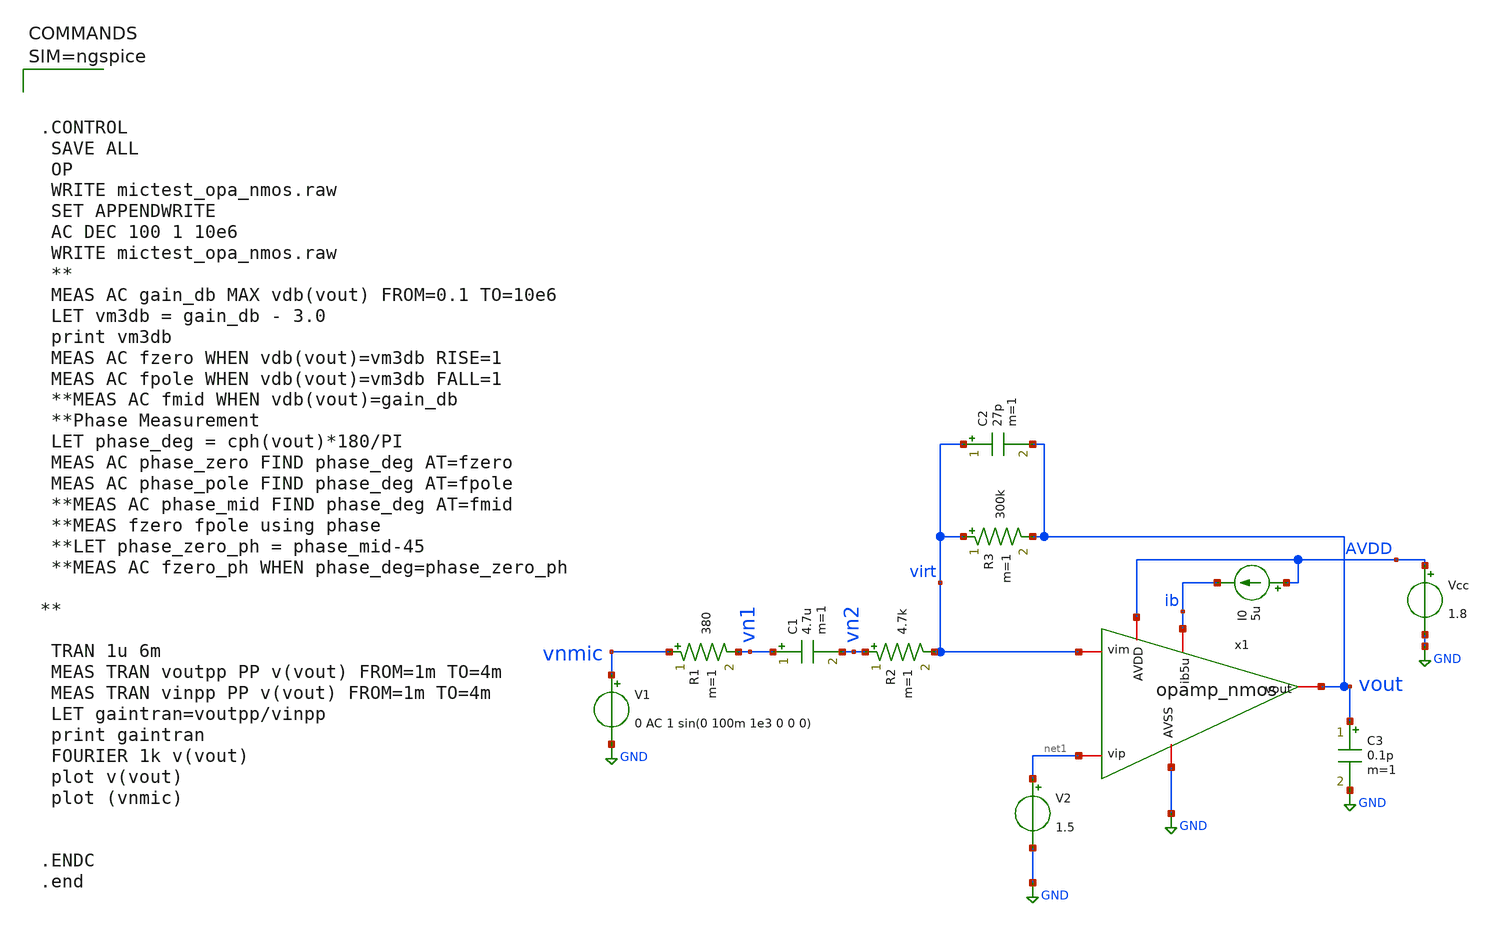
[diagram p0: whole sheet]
** sch_path: xschem/mictest_opa_nmos.sch
**.subckt mictest_opa_nmos
V1 vnmic GND 0 AC 1 sin(0 100m 1e3 0 0 0)
C1 vn1 vn2 4.7u m=1
R1 vnmic vn1 380 m=1
R2 vn2 virt 4.7k m=1
R3 virt vout 300k m=1
C2 virt vout 27p m=1
C3 vout GND 0.1p m=1
V2 net1 GND 1.5
x1 net1 GND AVDD virt ib vout opamp_nmos
Vcc AVDD GND 1.8
I0 AVDD ib 5u
**** begin user architecture code




.CONTROL
 SAVE ALL
 OP
 WRITE mictest_opa_nmos.raw
 SET APPENDWRITE
 AC DEC 100 1 10e6
 WRITE mictest_opa_nmos.raw
 **
 MEAS AC gain_db MAX vdb(vout) FROM=0.1 TO=10e6
 LET vm3db = gain_db - 3.0
 print vm3db
 MEAS AC fzero WHEN vdb(vout)=vm3db RISE=1
 MEAS AC fpole WHEN vdb(vout)=vm3db FALL=1
 **MEAS AC fmid WHEN vdb(vout)=gain_db
 **Phase Measurement
 LET phase_deg = cph(vout)*180/PI
 MEAS AC phase_zero FIND phase_deg AT=fzero
 MEAS AC phase_pole FIND phase_deg AT=fpole
 **MEAS AC phase_mid FIND phase_deg AT=fmid
 **MEAS fzero fpole using phase
 **LET phase_zero_ph = phase_mid-45
 **MEAS AC fzero_ph WHEN phase_deg=phase_zero_ph

**

 TRAN 1u 6m
 MEAS TRAN voutpp PP v(vout) FROM=1m TO=4m
 MEAS TRAN vinpp PP v(vout) FROM=1m TO=4m
 LET gaintran=voutpp/vinpp
 print gaintran
 FOURIER 1k v(vout)
 plot v(vout)
 plot (vnmic)


.ENDC
.end




** opencircuitdesign pdks install
.lib $::SKYWATER_MODELS/sky130.lib.spice tt

**** end user architecture code
**.ends

* expanding   symbol:  opamp_nmos.sym # of pins=6
** sym_path: xschem/opamp_nmos.sym
** sch_path: xschem/opamp_nmos.sch
.subckt opamp_nmos vip AVSS AVDD vim ib5u vout
*.iopin vip
*.iopin vim
*.iopin vout
*.iopin AVDD
*.iopin ib5u
*.iopin AVSS
XMip vom vip net1 net1 sky130_fd_pr__nfet_01v8_lvt L=2 W=5 nf=1 ad='int((1 + 1)/2) * 5 / 1 * 0.29' as='int((1 + 2)/2) * 5 / 1 * 0.29'
+ pd='2*int((1 + 1)/2) * (5 / 1 + 0.29)' ps='2*int((1 + 2)/2) * (5 / 1 + 0.29)' nrd='0.29 / 5 ' nrs='0.29 / 5 '
+ sa=0 sb=0 sd=0 mult=4 m=4
XMim vout vim net1 net1 sky130_fd_pr__nfet_01v8_lvt L=2 W=5 nf=1 ad='int((1 + 1)/2) * 5 / 1 * 0.29' as='int((1 + 2)/2) * 5 / 1 * 0.29'
+ pd='2*int((1 + 1)/2) * (5 / 1 + 0.29)' ps='2*int((1 + 2)/2) * (5 / 1 + 0.29)' nrd='0.29 / 5 ' nrs='0.29 / 5 '
+ sa=0 sb=0 sd=0 mult=4 m=4
XM1 ib5u ib5u AVSS AVSS sky130_fd_pr__nfet_01v8 L=1 W=5 nf=1 ad='int((1 + 1)/2) * 5 / 1 * 0.29' as='int((1 + 2)/2) * 5 / 1 * 0.29'
+ pd='2*int((1 + 1)/2) * (5 / 1 + 0.29)' ps='2*int((1 + 2)/2) * (5 / 1 + 0.29)' nrd='0.29 / 5 ' nrs='0.29 / 5 '
+ sa=0 sb=0 sd=0 mult=1 m=1
XMtail net1 ib5u AVSS AVSS sky130_fd_pr__nfet_01v8 L=1 W=5 nf=1 ad='int((1 + 1)/2) * 5 / 1 * 0.29' as='int((1 + 2)/2) * 5 / 1 * 0.29'
+ pd='2*int((1 + 1)/2) * (5 / 1 + 0.29)' ps='2*int((1 + 2)/2) * (5 / 1 + 0.29)' nrd='0.29 / 5 ' nrs='0.29 / 5 '
+ sa=0 sb=0 sd=0 mult=2 m=2
XMpcmp vom vom AVDD AVDD sky130_fd_pr__pfet_01v8_lvt L=2 W=5 nf=1 ad='int((1 + 1)/2) * 5 / 1 * 0.29'
+ as='int((1 + 2)/2) * 5 / 1 * 0.29' pd='2*int((1 + 1)/2) * (5 / 1 + 0.29)' ps='2*int((1 + 2)/2) * (5 / 1 + 0.29)'
+ nrd='0.29 / 5 ' nrs='0.29 / 5 ' sa=0 sb=0 sd=0 mult=2 m=2
XMpcmm vout vom AVDD AVDD sky130_fd_pr__pfet_01v8_lvt L=2 W=5 nf=1 ad='int((1 + 1)/2) * 5 / 1 * 0.29'
+ as='int((1 + 2)/2) * 5 / 1 * 0.29' pd='2*int((1 + 1)/2) * (5 / 1 + 0.29)' ps='2*int((1 + 2)/2) * (5 / 1 + 0.29)'
+ nrd='0.29 / 5 ' nrs='0.29 / 5 ' sa=0 sb=0 sd=0 mult=2 m=2
.ends

.GLOBAL GND
.end
